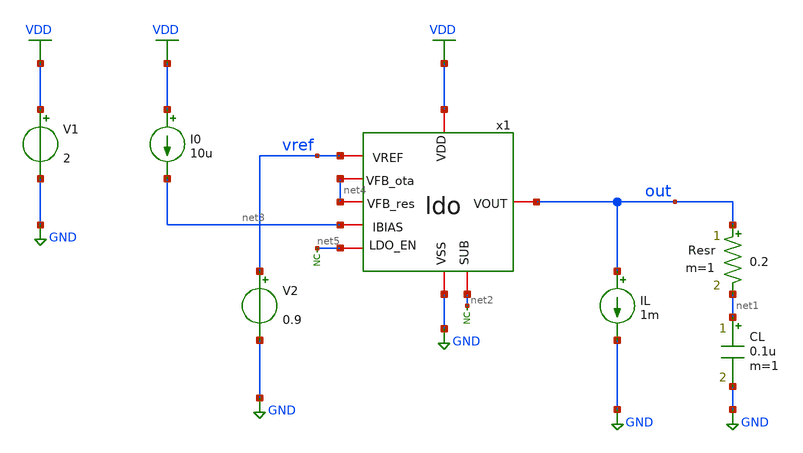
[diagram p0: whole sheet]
** sch_path: designs/libs/tb_ldo/tb_ldo/tb_ldo.sch
**.subckt tb_ldo
* noconn #net5
V1 VDD GND 2
V2 vref GND 0.9
I0 VDD net3 10u
CL net1 GND 0.1u m=1
Resr out net1 0.2 m=1
x1 VDD vref out net3 net2 GND net5 net4 net4 ldo
* noconn #net2
IL out GND 1m
**** begin user architecture code



.control
save all

run
set color0 = white

** Simulations Temperature and Line Regulation
dc TEMP -40 125 1  V1 2 5 0.25

** Measurements
meas dc Vout_max MAX v(out)
meas dc Vout_min MIN v(out)
let dev_max = abs(Vout_max - 1.8)
print dev_max
let dev_min = abs(Vout_min - 1.8)
print dev_min
let Vout_acc_abs = max(dev_max, dev_min)
print Vout_acc_abs
let Vout_acc_rel = (Vout_acc_abs / 1.8) * 100
print Vout_acc_rel

** Plots
setplot dc1
let vout=v(out)
plot vout

write tb_ldo.raw

.endc
* ngspice commands




.include $::180MCU_MODELS/design.ngspice
.lib $::180MCU_MODELS/sm141064.ngspice typical
.lib $::180MCU_MODELS/sm141064.ngspice cap_mim
.lib $::180MCU_MODELS/sm141064.ngspice moscap_typical
.lib $::180MCU_MODELS/sm141064.ngspice mimcap_typical
.lib $::180MCU_MODELS/sm141064.ngspice res_typical
* .lib $::180MCU_MODELS/sm141064.ngspice res_statistical
* ngspice commands

**** end user architecture code
**.ends
.GLOBAL GND
.GLOBAL VDD
.end
